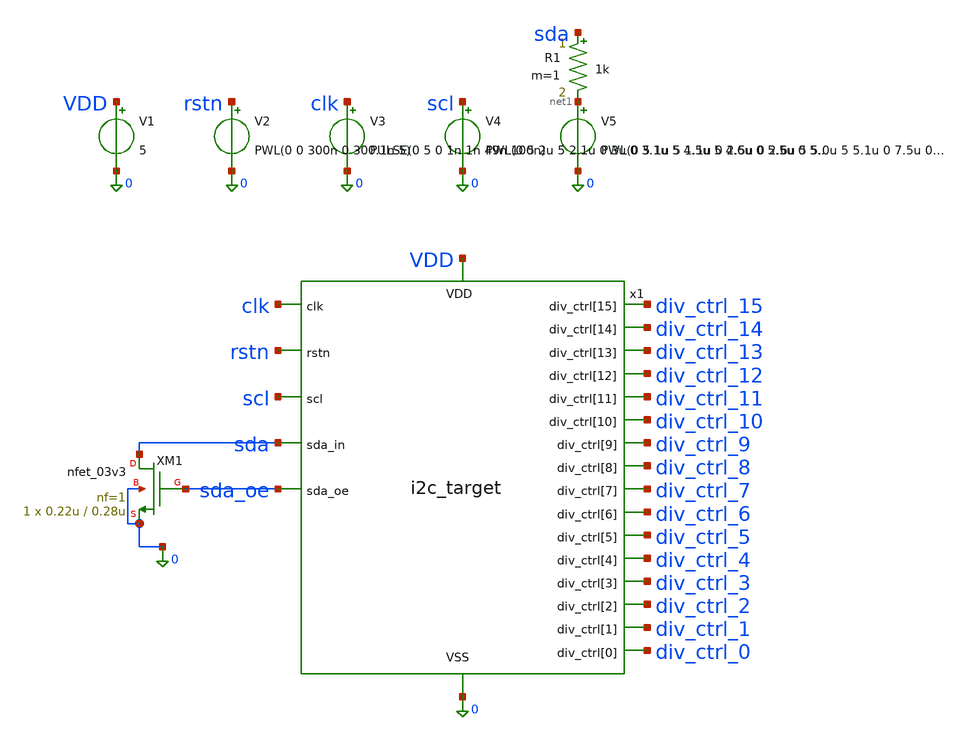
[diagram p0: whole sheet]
** sch_path: designs/libs/tb_analog/tb_i2c/tb_i2c.sch
**.subckt tb_i2c
V1 VDD 0 5
V2 rstn 0 PWL(0 0 300n 0 300.1n 5)
V3 clk 0 PULSE(0 5 0 1n 1n 49n 100n)
V4 scl 0 PWL(0 5 2u 5 2.1u 0 3u 0 3.1u 5 4.5u 5 4.6u 0 5.5u 0 5.6u 5 7.0u 5 7.1u 0 8.0u 0 8.1u 5
+ 9.5u 5 9.6u 0 10.5u 0 10.6u 5 12.0u 5 12.1u 0 13.0u 0 13.1u 5 14.5u 5 14.6u 0 15.5u 0 15.6u 5 17.0u 5
+ 17.1u 0 18.0u 0 18.1u 5 19.5u 5 19.6u 0 20.5u 0 20.6u 5 22.0u 5 22.1u 0 23.0u 0 23.1u 5 24.5u 5 24.6u 0
+ 25.5u 0 25.6u 5 27.0u 5 27.1u 0 28.0u 0 28.1u 5 29.5u 5 29.6u 0 30.5u 0 30.6u 5 32.0u 5 32.1u 0 33.0u 0
+ 33.1u 5 34.5u 5 34.6u 0 35.5u 0 35.6u 5 37.0u 5 37.1u 0 38.0u 0 38.1u 5 39.5u 5 39.6u 0 40.5u 0 40.6u 5
+ 42.0u 5 42.1u 0 43.0u 0 43.1u 5 44.5u 5 44.6u 0 45.5u 0 45.6u 5 47.0u 5 47.1u 0 48.0u 0 48.1u 5 50u 5)
V5 net1 0 PWL(0 5 1u 5 1.1u 0 2.5u 0 2.6u 5 5.0u 5 5.1u 0 7.5u 0 7.6u 5 10.0u 5 10.1u 0 12.5u 0
+ 12.6u 0 15.0u 0 15.1u 0 17.5u 0 17.6u 0 20.0u 0 20.1u 0 22.5u 0 22.6u 5 25.0u 5 25.1u 5 27.5u 5 27.6u 5
+ 30.0u 5 30.1u 0 32.5u 0 32.6u 0 35.0u 0 35.1u 5 37.5u 5 37.6u 5 40.0u 5 40.1u 0 42.5u 0 42.6u 0 45.0u 0
+ 45.1u 5 47.5u 5 47.6u 0 48.5u 0 48.6u 5)
R1 sda net1 1k m=1
XM1 sda sda_oe 0 0 nfet_03v3 L=0.28u W=0.22u nf=1 ad='int((nf+1)/2) * W/nf * 0.18u' as='int((nf+2)/2) * W/nf * 0.18u'
+ pd='2*int((nf+1)/2) * (W/nf + 0.18u)' ps='2*int((nf+2)/2) * (W/nf + 0.18u)' nrd='0.18u / W' nrs='0.18u / W'
+ sa=0 sb=0 sd=0 m=1
x1 VDD 0 clk div_ctrl_0 div_ctrl_10 div_ctrl_11 div_ctrl_12 div_ctrl_13 div_ctrl_14 div_ctrl_15
+ div_ctrl_1 div_ctrl_2 div_ctrl_3 div_ctrl_4 div_ctrl_5 div_ctrl_6 div_ctrl_7 div_ctrl_8 div_ctrl_9 rstn scl
+ sda sda_oe i2c_target
**** begin user architecture code


* 1. Extracted SPICE Subcircuit (Ensure name matches LVS extraction)
.include /workspace/designs/libs/core_analog/I2C/i2c_target.spice
* 2. GF180 Standard Cell Library
.include /foss/pdks/gf180mcuD/libs.ref/gf180mcu_fd_sc_mcu7t5v0/spice/gf180mcu_fd_sc_mcu7t5v0.spice
* 3. Device Models
.include /foss/pdks/gf180mcuD/libs.tech/ngspice/design.ngspice
.lib /foss/pdks/gf180mcuD/libs.tech/ngspice/sm141064.ngspice typical

.tran 10n 55u
.save all
.control
  run
  * Plot 1: Input Stimulus (Notice SDA will dip slightly below 5V when ACK'd)
  plot v(scl)+6 v(sda) v(sda_oe)-6
  * Plot 2: Output Bus (Cleaned up without escaped brackets!)
  plot v(div_ctrl_15)+30 v(div_ctrl_14)+28 v(div_ctrl_13)+26 v(div_ctrl_12)+24 v(div_ctrl_11)+22 v(div_ctrl_10)+20 v(div_ctrl_9)+18 v(div_ctrl_8)+16 v(div_ctrl_7)+14 v(div_ctrl_6)+12 v(div_ctrl_5)+10 v(div_ctrl_4)+8 v(div_ctrl_3)+6 v(div_ctrl_2)+4 v(div_ctrl_1)+2 v(div_ctrl_0)
.endc

**** end user architecture code
**.ends
.end
